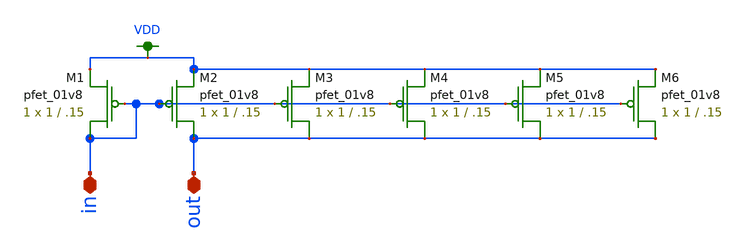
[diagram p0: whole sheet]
** sch_path: schemas/PMOS_gain_mirror.sch
**.subckt PMOS_gain_mirror in out
*.iopin in
*.iopin out
XM1 in in VDD VDD sky130_fd_pr__pfet_01v8 L=.15 W=1 nf=1 ad='int((nf+1)/2) * W/nf * 0.29' as='int((nf+2)/2) * W/nf * 0.29'
+ pd='2*int((nf+1)/2) * (W/nf + 0.29)' ps='2*int((nf+2)/2) * (W/nf + 0.29)' nrd='0.29 / W' nrs='0.29 / W'
+ sa=0 sb=0 sd=0 mult=1 m=1
XM2 out in VDD VDD sky130_fd_pr__pfet_01v8 L=.15 W=1 nf=1 ad='int((nf+1)/2) * W/nf * 0.29' as='int((nf+2)/2) * W/nf * 0.29'
+ pd='2*int((nf+1)/2) * (W/nf + 0.29)' ps='2*int((nf+2)/2) * (W/nf + 0.29)' nrd='0.29 / W' nrs='0.29 / W'
+ sa=0 sb=0 sd=0 mult=1 m=1
XM3 out in VDD VDD sky130_fd_pr__pfet_01v8 L=.15 W=1 nf=1 ad='int((nf+1)/2) * W/nf * 0.29' as='int((nf+2)/2) * W/nf * 0.29'
+ pd='2*int((nf+1)/2) * (W/nf + 0.29)' ps='2*int((nf+2)/2) * (W/nf + 0.29)' nrd='0.29 / W' nrs='0.29 / W'
+ sa=0 sb=0 sd=0 mult=1 m=1
XM4 out in VDD VDD sky130_fd_pr__pfet_01v8 L=.15 W=1 nf=1 ad='int((nf+1)/2) * W/nf * 0.29' as='int((nf+2)/2) * W/nf * 0.29'
+ pd='2*int((nf+1)/2) * (W/nf + 0.29)' ps='2*int((nf+2)/2) * (W/nf + 0.29)' nrd='0.29 / W' nrs='0.29 / W'
+ sa=0 sb=0 sd=0 mult=1 m=1
XM5 out in VDD VDD sky130_fd_pr__pfet_01v8 L=.15 W=1 nf=1 ad='int((nf+1)/2) * W/nf * 0.29' as='int((nf+2)/2) * W/nf * 0.29'
+ pd='2*int((nf+1)/2) * (W/nf + 0.29)' ps='2*int((nf+2)/2) * (W/nf + 0.29)' nrd='0.29 / W' nrs='0.29 / W'
+ sa=0 sb=0 sd=0 mult=1 m=1
XM6 out in VDD VDD sky130_fd_pr__pfet_01v8 L=.15 W=1 nf=1 ad='int((nf+1)/2) * W/nf * 0.29' as='int((nf+2)/2) * W/nf * 0.29'
+ pd='2*int((nf+1)/2) * (W/nf + 0.29)' ps='2*int((nf+2)/2) * (W/nf + 0.29)' nrd='0.29 / W' nrs='0.29 / W'
+ sa=0 sb=0 sd=0 mult=1 m=1
**.ends
.GLOBAL VDD
.end
